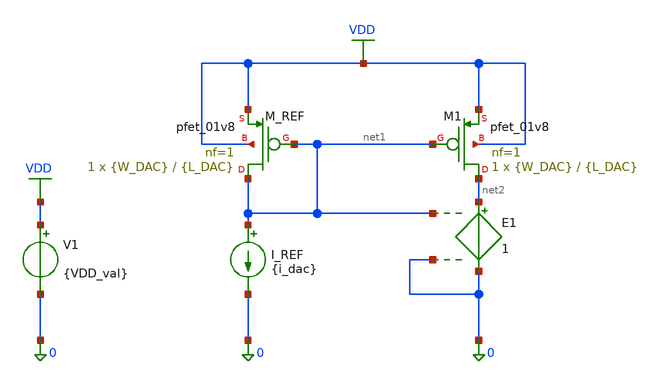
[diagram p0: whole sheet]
** sch_path: designs_backup/designs/lab2_mismatch.sch
**.subckt lab2_mismatch
XM1 net2 net1 VDD VDD sky130_fd_pr__pfet_01v8 L={L_DAC} W={W_DAC} nf=1 ad='int((1 + 1)/2) * {W_DAC} / 1 * 0.29'
+ as='int((1 + 2)/2) * {W_DAC} / 1 * 0.29' pd='2*int((1 + 1)/2) * ({W_DAC} / 1 + 0.29)' ps='2*int((1 + 2)/2) * ({W_DAC} / 1 + 0.29)'
+ nrd='0.29 / {W_DAC} ' nrs='0.29 / {W_DAC} ' sa=0 sb=0 sd=0 mult=1 m=1
XM_REF net1 net1 VDD VDD sky130_fd_pr__pfet_01v8 L={L_DAC} W={W_DAC} nf=1 ad='int((1 + 1)/2) * {W_DAC} / 1 * 0.29'
+ as='int((1 + 2)/2) * {W_DAC} / 1 * 0.29' pd='2*int((1 + 1)/2) * ({W_DAC} / 1 + 0.29)' ps='2*int((1 + 2)/2) * ({W_DAC} / 1 + 0.29)'
+ nrd='0.29 / {W_DAC} ' nrs='0.29 / {W_DAC} ' sa=0 sb=0 sd=0 mult=1 m=1
I_REF net1 0 {i_dac}
E1 net2 0 net1 0 1
V1 VDD 0 {VDD_val}
**** begin user architecture code

.lib $PDK_ROOT/sky130A/libs.tech/ngspice/sky130.lib.spice tt
.options savecurrents
.param W_DAC = 1.0
.param L_DAC = 0.2
.param i_dac = 10u
.param VDD_val = 1.8
.save all

.control
  foreach current_val 1u 2u 3u 4u 5u 6u 7u 8u 9u 10u
    alterparam i_dac = $current_val
    reset
    dc V1 1.8 1.9 0.1
    let net1v = v(net1)
    echo For

**** end user architecture code
**.ends
.GLOBAL VDD
.end
